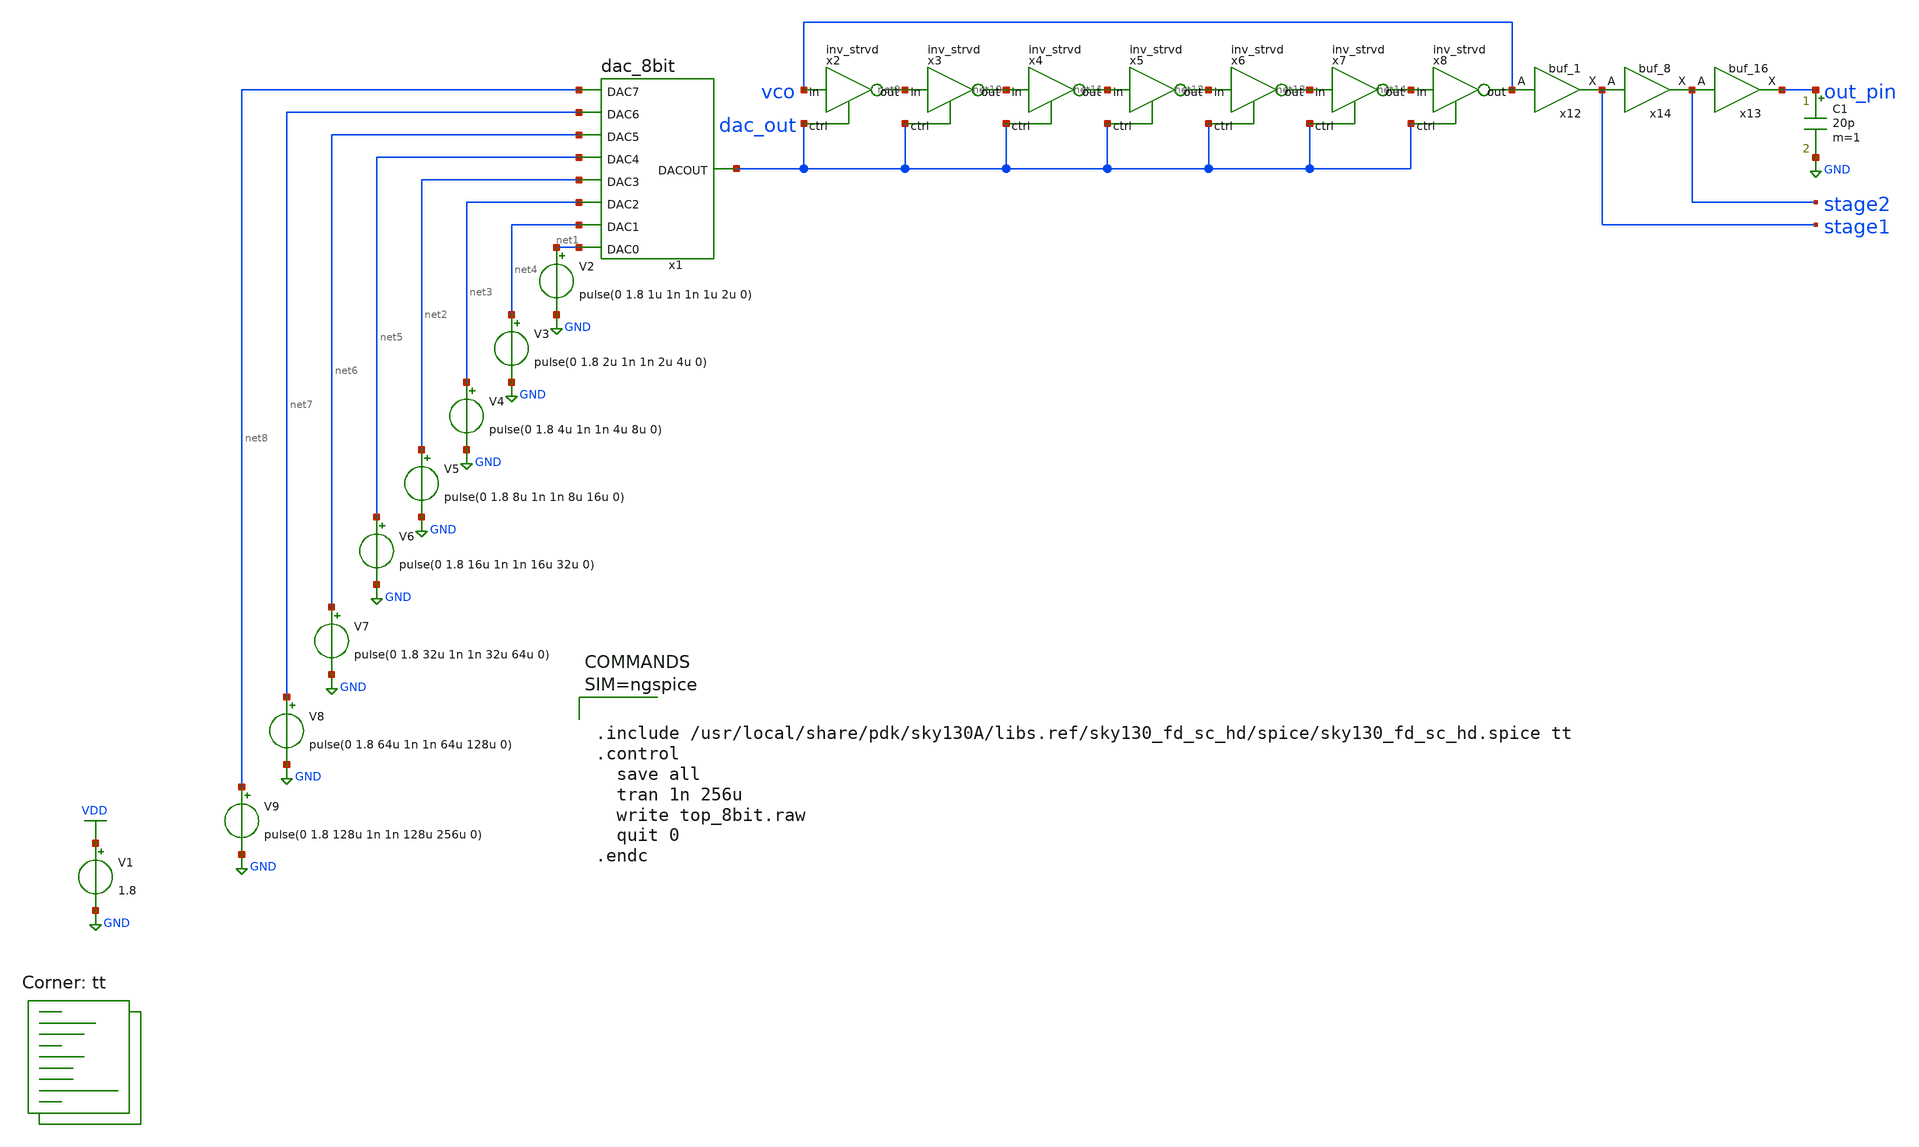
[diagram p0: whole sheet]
** sch_path: archive/tt_um_wulf_8bit_vco/xschem/top_8bit.sch
**.subckt top_8bit
V1 VDD GND 1.8
V2 net1 GND pulse(0 1.8 1u 1n 1n 1u 2u 0)
V3 net4 GND pulse(0 1.8 2u 1n 1n 2u 4u 0)
V4 net3 GND pulse(0 1.8 4u 1n 1n 4u 8u 0)
V5 net2 GND pulse(0 1.8 8u 1n 1n 8u 16u 0)
x2 vco net9 dac_out VDD GND inv_strvd
x3 net9 net10 dac_out VDD GND inv_strvd
x4 net10 net11 dac_out VDD GND inv_strvd
x5 net11 net12 dac_out VDD GND inv_strvd
x6 net12 net13 dac_out VDD GND inv_strvd
x7 net13 net14 dac_out VDD GND inv_strvd
x8 net14 vco dac_out VDD GND inv_strvd
x1 dac_out net2 net3 net4 net1 net8 net7 net6 net5 VDD GND dac_8bit
V6 net5 GND pulse(0 1.8 16u 1n 1n 16u 32u 0)
V7 net6 GND pulse(0 1.8 32u 1n 1n 32u 64u 0)
V8 net7 GND pulse(0 1.8 64u 1n 1n 64u 128u 0)
V9 net8 GND pulse(0 1.8 128u 1n 1n 128u 256u 0)
C1 out_pin GND 20p m=1
x12 vco GND GND VDD VDD stage1 sky130_fd_sc_hd__buf_1
x13 stage2 GND GND VDD VDD out_pin sky130_fd_sc_hd__buf_16
x14 stage1 GND GND VDD VDD stage2 sky130_fd_sc_hd__buf_8
**** begin user architecture code



.include /usr/local/share/pdk/sky130A/libs.ref/sky130_fd_sc_hd/spice/sky130_fd_sc_hd.spice tt
.control
  save all
  tran 1n 256u
  write top_8bit.raw
  quit 0
.endc



.lib $::SKYWATER_MODELS/sky130.lib.spice tt
**** end user architecture code
**.ends

* expanding   symbol:  inv_strvd.sym # of pins=3
** sym_path: archive/tt_um_wulf_8bit_vco/xschem/lib/inv_strvd.sym
** sch_path: archive/tt_um_wulf_8bit_vco/xschem/lib/inv_strvd.sch
.subckt inv_strvd in out ctrl VDD VSS
*.ipin in
*.ipin ctrl
*.opin out
XM2 out in net1 net1 sky130_fd_pr__nfet_01v8 L=1 W=40 nf=1 ad='int((1 + 1)/2) * 40 / 1 * 0.29' as='int((1 + 2)/2) * 40 / 1 * 0.29'
+ pd='2*int((1 + 1)/2) * (40 / 1 + 0.29)' ps='2*int((1 + 2)/2) * (40 / 1 + 0.29)' nrd='0.29 / 40 ' nrs='0.29 / 40 '
+ sa=0 sb=0 sd=0 mult=1 m=1
XM3 net1 ctrl VSS VSS sky130_fd_pr__nfet_01v8 L=0.15 W=1 nf=1 ad='int((1 + 1)/2) * 1 / 1 * 0.29' as='int((1 + 2)/2) * 1 / 1 * 0.29'
+ pd='2*int((1 + 1)/2) * (1 / 1 + 0.29)' ps='2*int((1 + 2)/2) * (1 / 1 + 0.29)' nrd='0.29 / 1 ' nrs='0.29 / 1 '
+ sa=0 sb=0 sd=0 mult=1 m=1
XM1 out in VDD VDD sky130_fd_pr__pfet_01v8 L=4 W=40 nf=1 ad='int((nf+1)/2) * W/nf * 0.29' as='int((nf+2)/2) * W/nf * 0.29'
+ pd='2*int((nf+1)/2) * (W/nf + 0.29)' ps='2*int((nf+2)/2) * (W/nf + 0.29)' nrd='0.29 / W' nrs='0.29 / W'
+ sa=0 sb=0 sd=0 mult=1 m=1
.ends


* expanding   symbol:  dac_8bit.sym # of pins=9
** sym_path: archive/tt_um_wulf_8bit_vco/xschem/lib/dac_8bit.sym
** sch_path: archive/tt_um_wulf_8bit_vco/xschem/lib/dac_8bit.sch
.subckt dac_8bit DACOUT DAC3 DAC2 DAC1 DAC0 DAC7 DAC6 DAC5 DAC4 VDD VSS
*.ipin DAC3
*.ipin DAC2
*.ipin DAC1
*.ipin DAC0
*.opin DACOUT
*.ipin DAC4
*.ipin DAC5
*.ipin DAC6
*.ipin DAC7
XR1 net3 VSS VSS sky130_fd_pr__res_xhigh_po_0p35 L=0.5 mult=1 m=1
XR2 DAC0 net3 VSS sky130_fd_pr__res_xhigh_po_0p35 L=0.5 mult=1 m=1
XR3 net2 net3 VSS sky130_fd_pr__res_xhigh_po_0p35 L=0.25 mult=1 m=1
XR4 DAC1 net2 VSS sky130_fd_pr__res_xhigh_po_0p35 L=0.5 mult=1 m=1
XR5 net1 net2 VSS sky130_fd_pr__res_xhigh_po_0p35 L=0.25 mult=1 m=1
XR6 DAC2 net1 VSS sky130_fd_pr__res_xhigh_po_0p35 L=0.5 mult=1 m=1
XR7 net5 net1 VSS sky130_fd_pr__res_xhigh_po_0p35 L=0.25 mult=1 m=1
XR8 DAC3 net5 VSS sky130_fd_pr__res_xhigh_po_0p35 L=0.5 mult=1 m=1
XR9 VDD DACOUT VSS sky130_fd_pr__res_xhigh_po_0p35 L=0.25 mult=1 m=1
XR10 net4 net5 VSS sky130_fd_pr__res_xhigh_po_0p35 L=0.25 mult=1 m=1
XR11 DAC4 net4 VSS sky130_fd_pr__res_xhigh_po_0p35 L=0.5 mult=1 m=1
XR12 net6 net4 VSS sky130_fd_pr__res_xhigh_po_0p35 L=0.25 mult=1 m=1
XR13 DAC5 net6 VSS sky130_fd_pr__res_xhigh_po_0p35 L=0.5 mult=1 m=1
XR14 net7 net6 VSS sky130_fd_pr__res_xhigh_po_0p35 L=0.25 mult=1 m=1
XR15 DAC6 net7 VSS sky130_fd_pr__res_xhigh_po_0p35 L=0.5 mult=1 m=1
XR16 DACOUT net7 VSS sky130_fd_pr__res_xhigh_po_0p35 L=0.25 mult=1 m=1
XR17 DAC7 DACOUT VSS sky130_fd_pr__res_xhigh_po_0p35 L=0.5 mult=1 m=1
.ends

.GLOBAL GND
.GLOBAL VDD
.end
